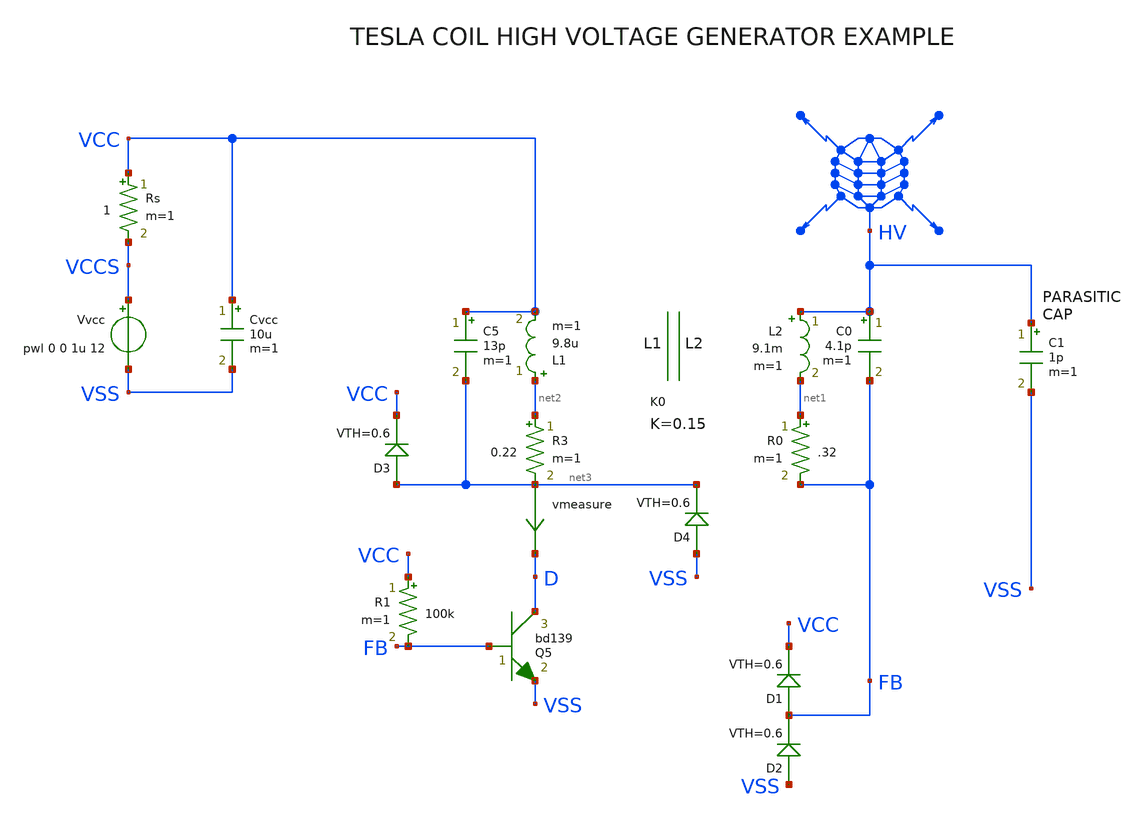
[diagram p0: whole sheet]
** sch_path: xschem_library/examples/tesla.sch
**.subckt tesla
Rs VCC VCCS 1 m=1
Vvcc VCCS VSS pwl 0 0 1u 12
Cvcc VCC VSS 10u m=1
C1 HV VSS 1p m=1
L1 net2 VCC 9.8u m=1
L2 HV net1 9.1m m=1
K0 L1 L2 0.15
R0 net1 FB .32 m=1
C0 HV FB 4.1p m=1
R3 net2 net3 0.22 m=1
C5 VCC net3 13p m=1
D2 VSS FB diode VTH=0.6 RON=10 ROFF=1G
D1 FB VCC diode VTH=0.6 RON=10 ROFF=1G
Q5 D FB VSS bd139 area=1 m=1
R1 VCC FB 100k m=1
D3 net3 VCC diode VTH=0.6 RON=10 ROFF=1G
vmeasure net3 D 0
.save i(vmeasure)
D4 VSS net3 diode VTH=0.6 RON=10 ROFF=1G
**** begin user architecture code

.option SCALE=1e-6 PARHIER=LOCAL RUNLVL=6 post MODMONTE=1
.option sampling_method = SRS
.option method=gear
vvss vss 0 dc 0

.save all

** models are generally not free: you must download
** SPICE models for active devices and put them  into the below
** referenced file in netlist/simulation directory.
.include models_tesla.txt
.temp 30
.tran 1n 1m  uic
.meas tran iavg AVG i(vc) from=950u to=990u
.probe tran p(q1) i(d2) i(d1) i(d3) i(l1) i(l2) i(L3)
.meas tran pavg AVG p(q1) from=950u to=990u


**** end user architecture code
**.ends
.end
